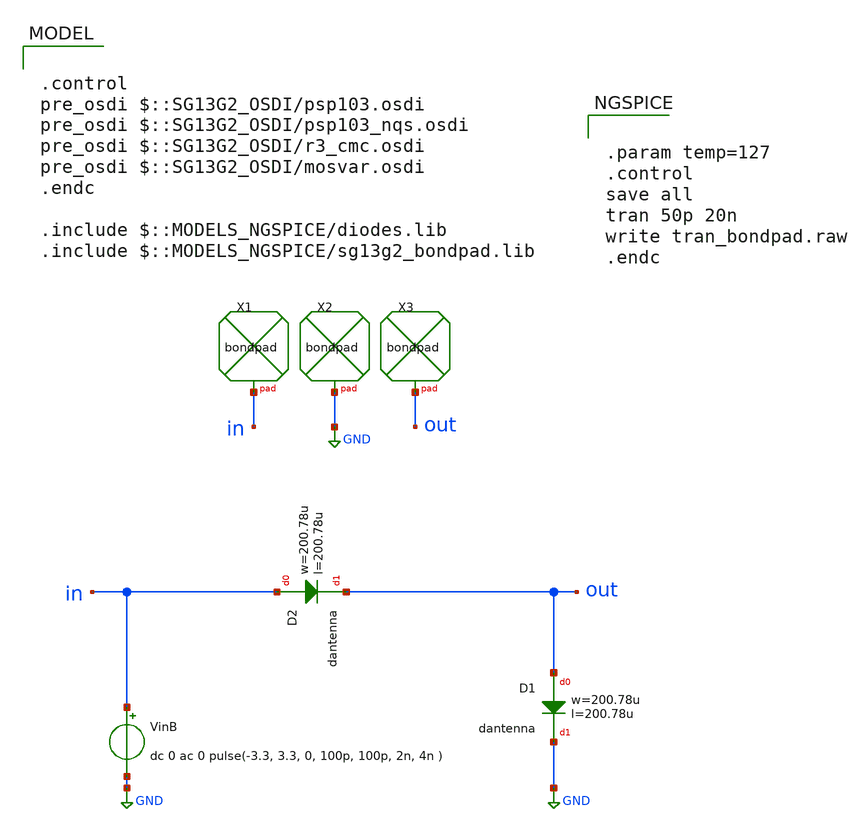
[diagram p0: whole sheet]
** sch_path: ihp-sg13g2/xschem_libs/sg13g2_tests/tran_bondpad/schematic/tran_bondpad.sch
* Copyright 2023 IHP PDK Authors
**.subckt tran_bondpad
VinB in GND dc 0 ac 0 pulse(-3.3, 3.3, 0, 100p, 100p, 2n, 4n )
XD1 out GND dantenna l=200.78u w=200.78u
XD2 in out dantenna l=200.78u w=200.78u
XX1 in bondpad size=80u shape=0 padtype=0
XX2 GND bondpad size=80u shape=0 padtype=0
XX3 out bondpad size=80u shape=0 padtype=0
**** begin user architecture code

.control
pre_osdi $::SG13G2_OSDI/psp103.osdi
pre_osdi $::SG13G2_OSDI/psp103_nqs.osdi
pre_osdi $::SG13G2_OSDI/r3_cmc.osdi
pre_osdi $::SG13G2_OSDI/mosvar.osdi
.endc

.include $::MODELS_NGSPICE/diodes.lib
.include $::MODELS_NGSPICE/sg13g2_bondpad.lib



.param temp=127
.control
save all
tran 50p 20n
write tran_bondpad.raw
.endc


**** end user architecture code
**.ends
.GLOBAL GND
.end
